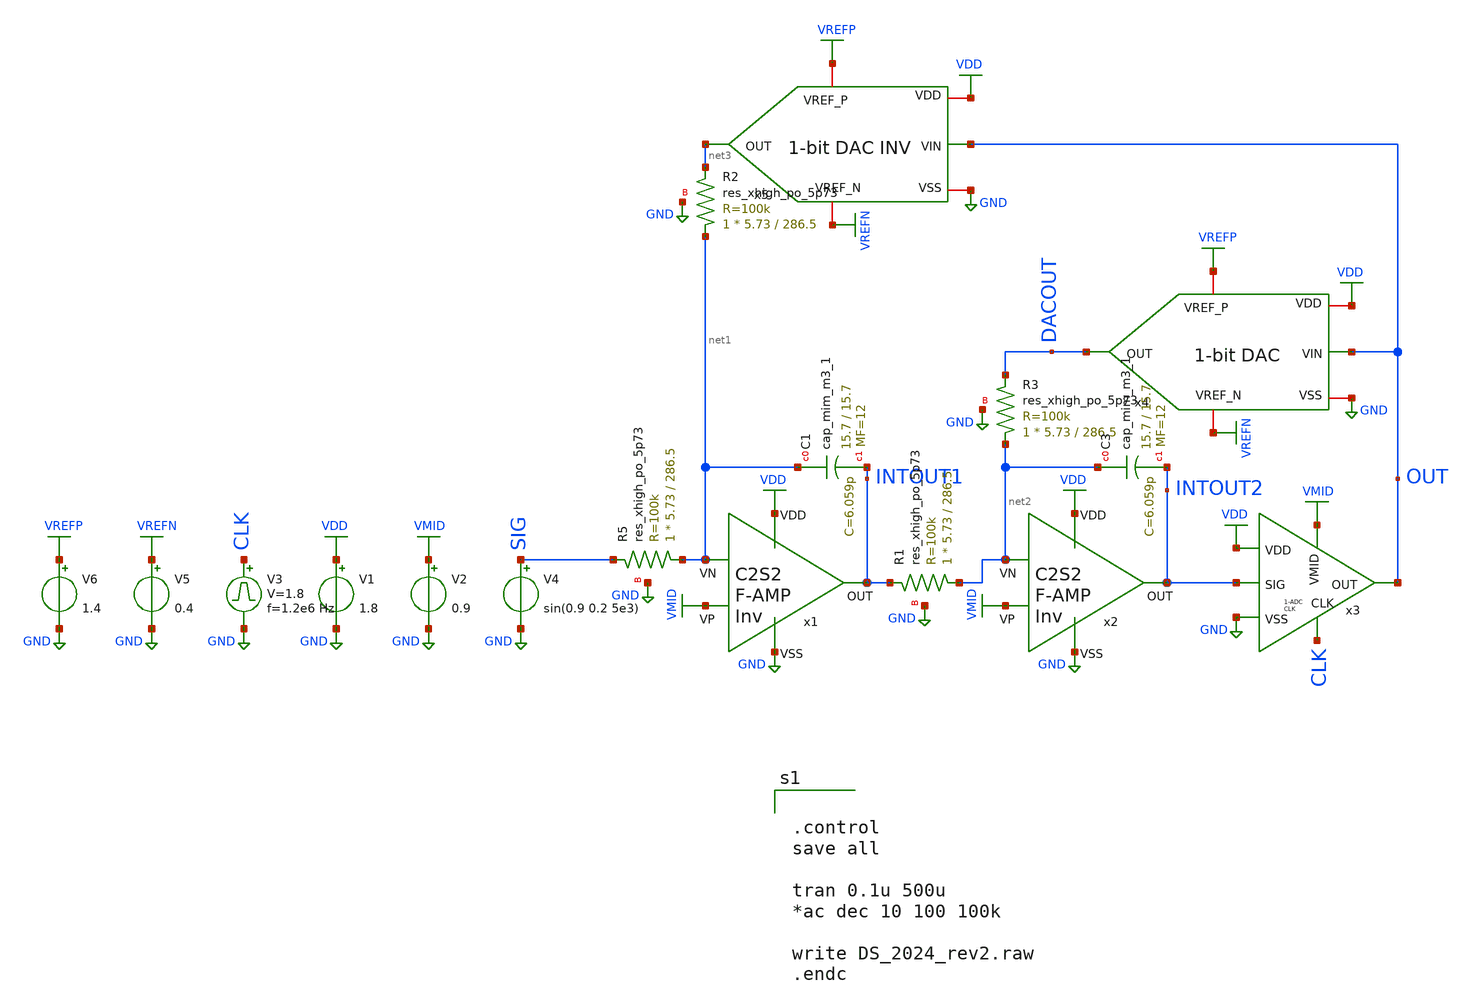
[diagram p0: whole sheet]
** sch_path: SP24_caravel_user_project_analog/xschem/xschem_DeltaSigma/DS_2024_2p2.sch
.lib $::SKYWATER_MODELS/sky130.lib.spice tt
.include $::SKYWATER_STDCELLS/sky130_fd_sc_hd.spice

**.subckt DS_2024_2p2
V1 VDD GND 1.8
V2 VMID GND 0.9
V3 CLK GND pulse 0 1.8 '0.495/ 1.2e6 ' '0.01/1.2e6 ' '0.01/1.2e6 ' '0.49/1.2e6 ' '1/1.2e6 '
V4 SIG GND sin(0.9 0.2 5e3)
V5 VREFN GND 0.4
V6 VREFP GND 1.4
x1 VDD VMID net1 INTOUT1 GND C2S2_Amp_F_I
x2 VDD VMID net2 INTOUT2 GND C2S2_Amp_F_I
x5 VREFP VDD net3 OUT GND VREFN 1Bit_DAC_Inv
x4 VREFP VDD DACOUT OUT GND VREFN 1Bit_DAC
x3 VDD INTOUT2 OUT CLK GND VMID 1Bit_Clk_ADC
XR5 net1 SIG GND sky130_fd_pr__res_xhigh_po_5p73 L=286.5 mult=1 m=1
XR1 net2 INTOUT1 GND sky130_fd_pr__res_xhigh_po_5p73 L=286.5 mult=1 m=1
XR2 net1 net3 GND sky130_fd_pr__res_xhigh_po_5p73 L=286.5 mult=1 m=1
XR3 net2 DACOUT GND sky130_fd_pr__res_xhigh_po_5p73 L=286.5 mult=1 m=1
XC3 net2 INTOUT2 sky130_fd_pr__cap_mim_m3_1 W=15.7 L=15.7 MF=12 m=12
XC1 net1 INTOUT1 sky130_fd_pr__cap_mim_m3_1 W=15.7 L=15.7 MF=12 m=12
**** begin user architecture code


.control
save all

tran 0.1u 500u
*ac dec 10 100 100k

write DS_2024_rev2.raw
.endc


**** end user architecture code
**.ends
.GLOBAL VDD
.GLOBAL GND
.GLOBAL VMID
.GLOBAL VREFN
.GLOBAL VREFP
.end
